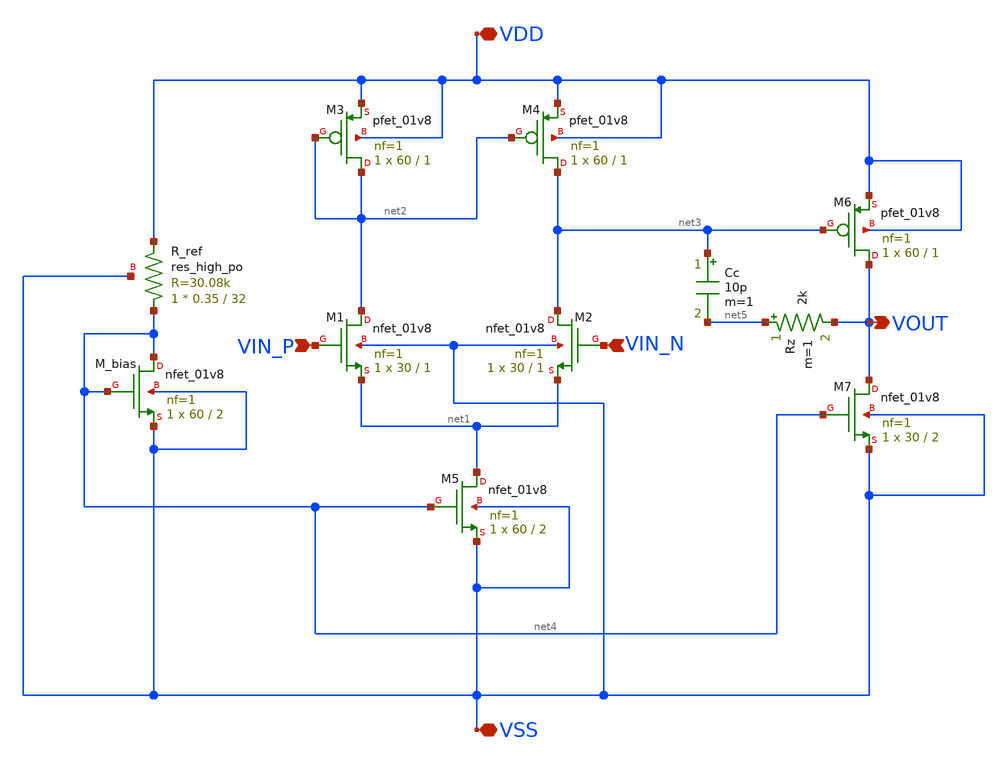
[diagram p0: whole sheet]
** sch_path: analog/schematics/opamp_two_stage(1).sch
**.subckt opamp_two_stage(1) VDD VSS VIN_P VIN_N VOUT
*.iopin VDD
*.iopin VSS
*.ipin VIN_P
*.ipin VIN_N
*.opin VOUT
XM1 net2 VIN_P net1 VSS sky130_fd_pr__nfet_01v8 L=1 W=30 nf=1 ad='int((nf+1)/2) * W/nf * 0.29' as='int((nf+2)/2) * W/nf * 0.29'
+ pd='2*int((nf+1)/2) * (W/nf + 0.29)' ps='2*int((nf+2)/2) * (W/nf + 0.29)' nrd='0.29 / W' nrs='0.29 / W'
+ sa=0 sb=0 sd=0 mult=1 m=1
XM2 net3 VIN_N net1 VSS sky130_fd_pr__nfet_01v8 L=1 W=30 nf=1 ad='int((nf+1)/2) * W/nf * 0.29' as='int((nf+2)/2) * W/nf * 0.29'
+ pd='2*int((nf+1)/2) * (W/nf + 0.29)' ps='2*int((nf+2)/2) * (W/nf + 0.29)' nrd='0.29 / W' nrs='0.29 / W'
+ sa=0 sb=0 sd=0 mult=1 m=1
XM3 net2 net2 VDD VDD sky130_fd_pr__pfet_01v8 L=1 W=60 nf=1 ad='int((nf+1)/2) * W/nf * 0.29' as='int((nf+2)/2) * W/nf * 0.29'
+ pd='2*int((nf+1)/2) * (W/nf + 0.29)' ps='2*int((nf+2)/2) * (W/nf + 0.29)' nrd='0.29 / W' nrs='0.29 / W'
+ sa=0 sb=0 sd=0 mult=1 m=1
XM4 net3 net2 VDD VDD sky130_fd_pr__pfet_01v8 L=1 W=60 nf=1 ad='int((nf+1)/2) * W/nf * 0.29' as='int((nf+2)/2) * W/nf * 0.29'
+ pd='2*int((nf+1)/2) * (W/nf + 0.29)' ps='2*int((nf+2)/2) * (W/nf + 0.29)' nrd='0.29 / W' nrs='0.29 / W'
+ sa=0 sb=0 sd=0 mult=1 m=1
XM5 net1 net4 VSS VSS sky130_fd_pr__nfet_01v8 L=2 W=60 nf=1 ad='int((nf+1)/2) * W/nf * 0.29' as='int((nf+2)/2) * W/nf * 0.29'
+ pd='2*int((nf+1)/2) * (W/nf + 0.29)' ps='2*int((nf+2)/2) * (W/nf + 0.29)' nrd='0.29 / W' nrs='0.29 / W'
+ sa=0 sb=0 sd=0 mult=1 m=1
XM6 VOUT net3 VDD VDD sky130_fd_pr__pfet_01v8 L=1 W=60 nf=1 ad='int((nf+1)/2) * W/nf * 0.29' as='int((nf+2)/2) * W/nf * 0.29'
+ pd='2*int((nf+1)/2) * (W/nf + 0.29)' ps='2*int((nf+2)/2) * (W/nf + 0.29)' nrd='0.29 / W' nrs='0.29 / W'
+ sa=0 sb=0 sd=0 mult=1 m=1
XM7 VOUT net4 VSS VSS sky130_fd_pr__nfet_01v8 L=2 W=30 nf=1 ad='int((nf+1)/2) * W/nf * 0.29' as='int((nf+2)/2) * W/nf * 0.29'
+ pd='2*int((nf+1)/2) * (W/nf + 0.29)' ps='2*int((nf+2)/2) * (W/nf + 0.29)' nrd='0.29 / W' nrs='0.29 / W'
+ sa=0 sb=0 sd=0 mult=1 m=1
XM_bias net4 net4 VSS VSS sky130_fd_pr__nfet_01v8 L=2 W=60 nf=1 ad='int((nf+1)/2) * W/nf * 0.29' as='int((nf+2)/2) * W/nf * 0.29'
+ pd='2*int((nf+1)/2) * (W/nf + 0.29)' ps='2*int((nf+2)/2) * (W/nf + 0.29)' nrd='0.29 / W' nrs='0.29 / W'
+ sa=0 sb=0 sd=0 mult=1 m=1
XR_ref net4 VDD VSS sky130_fd_pr__res_high_po W=0.35 L=32 mult=1 m=1
Cc net3 net5 10p m=1
Rz net5 VOUT 2k m=1
**.ends
.end
